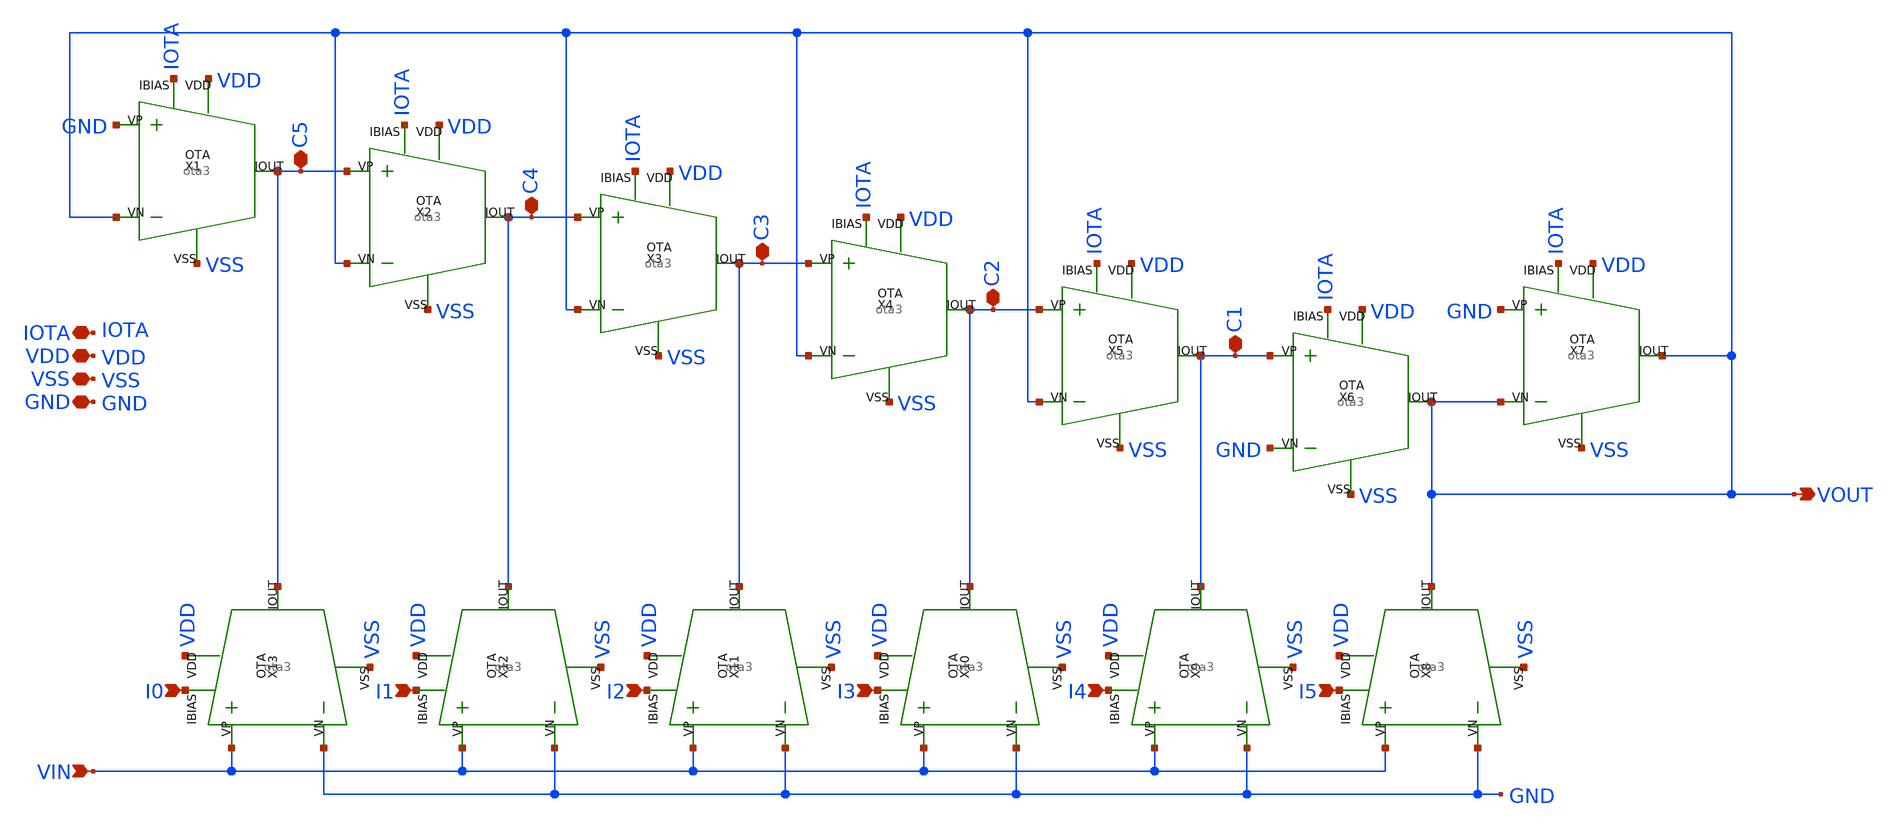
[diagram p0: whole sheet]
** sch_path: Fractional Order PID/Fractional Order Capacitor/Fractional_diff.sch
**.subckt Fractional_diff VIN I0 I1 I2 I3 I4 I5 IOTA VDD VSS GND VOUT C5 C4 C3 C2 C1
*.ipin VIN
*.ipin I0
*.ipin I1
*.ipin I2
*.ipin I3
*.ipin I4
*.ipin I5
*.iopin IOTA
*.iopin VDD
*.iopin VSS
*.iopin GND
*.opin VOUT
*.iopin C5
*.iopin C4
*.iopin C3
*.iopin C2
*.iopin C1
X1 IOTA VDD C5 VSS VOUT GND ota3
X2 IOTA VDD C4 VSS VOUT C5 ota3
X3 IOTA VDD C3 VSS VOUT C4 ota3
X4 IOTA VDD C2 VSS VOUT C3 ota3
X5 IOTA VDD C1 VSS VOUT C2 ota3
X6 IOTA VDD VOUT VSS GND C1 ota3
X7 IOTA VDD VOUT VSS VOUT GND ota3
X8 I5 VDD VOUT VSS GND VIN ota3
X9 I4 VDD C1 VSS GND VIN ota3
X10 I3 VDD C2 VSS GND VIN ota3
X11 I2 VDD C3 VSS GND VIN ota3
X12 I1 VDD C4 VSS GND VIN ota3
X13 I0 VDD C5 VSS GND VIN ota3
**.ends

* expanding   symbol:  /home/parallels/OTA/ota3.sym # of pins=6
** sym_path: Fractional Order PID/OTA/ota3.sym
** sch_path: Fractional Order PID/OTA/ota3.sch
.subckt ota3 IBIAS VDD IOUT VSS VN VP
*.iopin VP
*.iopin IBIAS
*.iopin IOUT
*.iopin VDD
*.iopin VSS
*.iopin VN
XMp1 net1 net1 VDD VDD sky130_fd_pr__pfet_01v8 L=2 W=10 nf=2 ad='int((nf+1)/2) * W/nf * 0.29' as='int((nf+2)/2) * W/nf * 0.29'
+ pd='2*int((nf+1)/2) * (W/nf + 0.29)' ps='2*int((nf+2)/2) * (W/nf + 0.29)' nrd='0.29 / W' nrs='0.29 / W'
+ sa=0 sb=0 sd=0 mult=1 m=1
XMp2 IOUT net1 VDD VDD sky130_fd_pr__pfet_01v8 L=2 W=10 nf=2 ad='int((nf+1)/2) * W/nf * 0.29' as='int((nf+2)/2) * W/nf * 0.29'
+ pd='2*int((nf+1)/2) * (W/nf + 0.29)' ps='2*int((nf+2)/2) * (W/nf + 0.29)' nrd='0.29 / W' nrs='0.29 / W'
+ sa=0 sb=0 sd=0 mult=1 m=1
XMn1 net1 VP net2 net2 sky130_fd_pr__nfet_01v8 L=5 W=25 nf=5 ad='int((nf+1)/2) * W/nf * 0.29' as='int((nf+2)/2) * W/nf * 0.29'
+ pd='2*int((nf+1)/2) * (W/nf + 0.29)' ps='2*int((nf+2)/2) * (W/nf + 0.29)' nrd='0.29 / W' nrs='0.29 / W'
+ sa=0 sb=0 sd=0 mult=1 m=1
XMn2 IOUT VN net2 net2 sky130_fd_pr__nfet_01v8 L=5 W=5 nf=1 ad='int((nf+1)/2) * W/nf * 0.29' as='int((nf+2)/2) * W/nf * 0.29'
+ pd='2*int((nf+1)/2) * (W/nf + 0.29)' ps='2*int((nf+2)/2) * (W/nf + 0.29)' nrd='0.29 / W' nrs='0.29 / W'
+ sa=0 sb=0 sd=0 mult=1 m=1
XMn3 net1 VP net3 net3 sky130_fd_pr__nfet_01v8 L=5 W=5 nf=1 ad='int((nf+1)/2) * W/nf * 0.29' as='int((nf+2)/2) * W/nf * 0.29'
+ pd='2*int((nf+1)/2) * (W/nf + 0.29)' ps='2*int((nf+2)/2) * (W/nf + 0.29)' nrd='0.29 / W' nrs='0.29 / W'
+ sa=0 sb=0 sd=0 mult=1 m=1
XMn4 IOUT VN net3 net3 sky130_fd_pr__nfet_01v8 L=5 W=25 nf=5 ad='int((nf+1)/2) * W/nf * 0.29' as='int((nf+2)/2) * W/nf * 0.29'
+ pd='2*int((nf+1)/2) * (W/nf + 0.29)' ps='2*int((nf+2)/2) * (W/nf + 0.29)' nrd='0.29 / W' nrs='0.29 / W'
+ sa=0 sb=0 sd=0 mult=1 m=1
XMb2 net2 IBIAS VSS VSS sky130_fd_pr__nfet_01v8 L=1.5 W=60 nf=12 ad='int((nf+1)/2) * W/nf * 0.29' as='int((nf+2)/2) * W/nf * 0.29'
+ pd='2*int((nf+1)/2) * (W/nf + 0.29)' ps='2*int((nf+2)/2) * (W/nf + 0.29)' nrd='0.29 / W' nrs='0.29 / W'
+ sa=0 sb=0 sd=0 mult=1 m=1
XMb1 IBIAS IBIAS VSS VSS sky130_fd_pr__nfet_01v8 L=1.5 W=60 nf=12 ad='int((nf+1)/2) * W/nf * 0.29' as='int((nf+2)/2) * W/nf * 0.29'
+ pd='2*int((nf+1)/2) * (W/nf + 0.29)' ps='2*int((nf+2)/2) * (W/nf + 0.29)' nrd='0.29 / W' nrs='0.29 / W'
+ sa=0 sb=0 sd=0 mult=1 m=1
XMb3 net3 IBIAS VSS VSS sky130_fd_pr__nfet_01v8 L=1.5 W=60 nf=12 ad='int((nf+1)/2) * W/nf * 0.29' as='int((nf+2)/2) * W/nf * 0.29'
+ pd='2*int((nf+1)/2) * (W/nf + 0.29)' ps='2*int((nf+2)/2) * (W/nf + 0.29)' nrd='0.29 / W' nrs='0.29 / W'
+ sa=0 sb=0 sd=0 mult=1 m=1
.ends

.end
